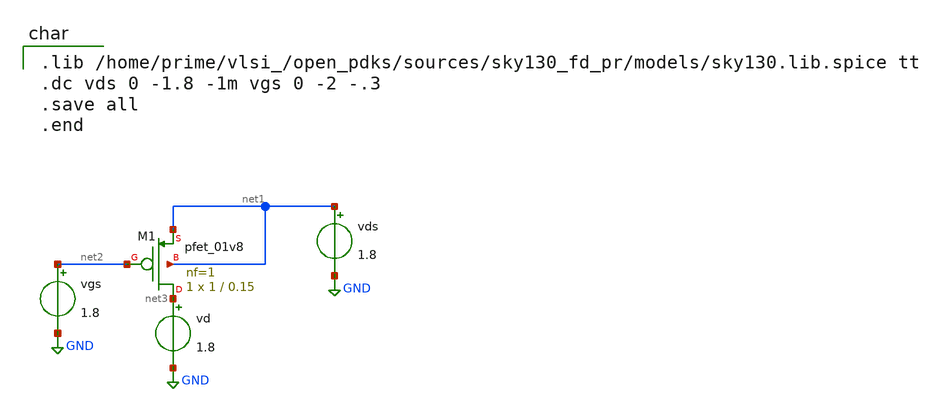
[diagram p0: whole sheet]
** sch_path: schematics/transient_simulation.sch
**.subckt transient_simulation
vds net1 GND 1.8
vgs net2 GND 1.8
XM1 net3 net2 net1 net1 sky130_fd_pr__pfet_01v8 L=0.15 W=1 nf=1 ad='int((1 + 1)/2) * 1 / 1 * 0.29' as='int((1 + 2)/2) * 1 / 1 * 0.29'
+ pd='2*int((1 + 1)/2) * (1 / 1 + 0.29)' ps='2*int((1 + 2)/2) * (1 / 1 + 0.29)' nrd='0.29 / 1 ' nrs='0.29 / 1 '
+ sa=0 sb=0 sd=0 mult=1 m=1
vd net3 GND 1.8
**** begin user architecture code

.lib /home/prime/vlsi_/open_pdks/sources/sky130_fd_pr/models/sky130.lib.spice tt
.dc vds 0 -1.8 -1m vgs 0 -2 -.3
.save all
.end

**** end user architecture code
**.ends
.GLOBAL GND
.end
